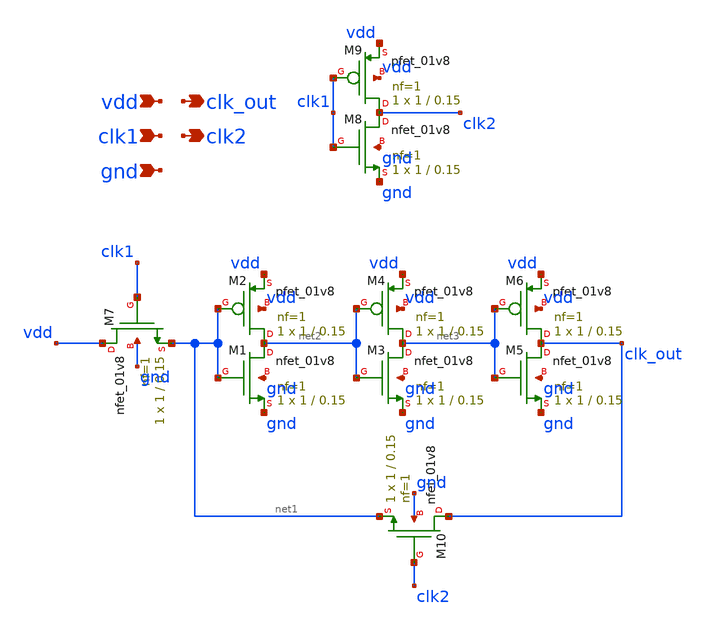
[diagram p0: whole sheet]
** sch_path: week3/xschem/ring_osc.sch
**.subckt ring_osc vdd gnd clk1 clk_out clk2
*.ipin vdd
*.ipin gnd
*.ipin clk1
*.opin clk_out
*.opin clk2
XM1 net2 net1 gnd gnd sky130_fd_pr__nfet_01v8 L=0.15 W=1 nf=1 ad='int((nf+1)/2) * W/nf * 0.29' as='int((nf+2)/2) * W/nf * 0.29'
+ pd='2*int((nf+1)/2) * (W/nf + 0.29)' ps='2*int((nf+2)/2) * (W/nf + 0.29)' nrd='0.29 / W' nrs='0.29 / W'
+ sa=0 sb=0 sd=0 mult=1 m=1
XM2 net2 net1 vdd vdd sky130_fd_pr__pfet_01v8 L=0.15 W=1 nf=1 ad='int((nf+1)/2) * W/nf * 0.29' as='int((nf+2)/2) * W/nf * 0.29'
+ pd='2*int((nf+1)/2) * (W/nf + 0.29)' ps='2*int((nf+2)/2) * (W/nf + 0.29)' nrd='0.29 / W' nrs='0.29 / W'
+ sa=0 sb=0 sd=0 mult=1 m=1
XM3 net3 net2 gnd gnd sky130_fd_pr__nfet_01v8 L=0.15 W=1 nf=1 ad='int((nf+1)/2) * W/nf * 0.29' as='int((nf+2)/2) * W/nf * 0.29'
+ pd='2*int((nf+1)/2) * (W/nf + 0.29)' ps='2*int((nf+2)/2) * (W/nf + 0.29)' nrd='0.29 / W' nrs='0.29 / W'
+ sa=0 sb=0 sd=0 mult=1 m=1
XM4 net3 net2 vdd vdd sky130_fd_pr__pfet_01v8 L=0.15 W=1 nf=1 ad='int((nf+1)/2) * W/nf * 0.29' as='int((nf+2)/2) * W/nf * 0.29'
+ pd='2*int((nf+1)/2) * (W/nf + 0.29)' ps='2*int((nf+2)/2) * (W/nf + 0.29)' nrd='0.29 / W' nrs='0.29 / W'
+ sa=0 sb=0 sd=0 mult=1 m=1
XM5 clk_out net3 gnd gnd sky130_fd_pr__nfet_01v8 L=0.15 W=1 nf=1 ad='int((nf+1)/2) * W/nf * 0.29' as='int((nf+2)/2) * W/nf * 0.29'
+ pd='2*int((nf+1)/2) * (W/nf + 0.29)' ps='2*int((nf+2)/2) * (W/nf + 0.29)' nrd='0.29 / W' nrs='0.29 / W'
+ sa=0 sb=0 sd=0 mult=1 m=1
XM6 clk_out net3 vdd vdd sky130_fd_pr__pfet_01v8 L=0.15 W=1 nf=1 ad='int((nf+1)/2) * W/nf * 0.29' as='int((nf+2)/2) * W/nf * 0.29'
+ pd='2*int((nf+1)/2) * (W/nf + 0.29)' ps='2*int((nf+2)/2) * (W/nf + 0.29)' nrd='0.29 / W' nrs='0.29 / W'
+ sa=0 sb=0 sd=0 mult=1 m=1
XM7 vdd clk1 net1 gnd sky130_fd_pr__nfet_01v8 L=0.15 W=1 nf=1 ad='int((nf+1)/2) * W/nf * 0.29' as='int((nf+2)/2) * W/nf * 0.29'
+ pd='2*int((nf+1)/2) * (W/nf + 0.29)' ps='2*int((nf+2)/2) * (W/nf + 0.29)' nrd='0.29 / W' nrs='0.29 / W'
+ sa=0 sb=0 sd=0 mult=1 m=1
XM8 clk2 clk1 gnd gnd sky130_fd_pr__nfet_01v8 L=0.15 W=1 nf=1 ad='int((nf+1)/2) * W/nf * 0.29' as='int((nf+2)/2) * W/nf * 0.29'
+ pd='2*int((nf+1)/2) * (W/nf + 0.29)' ps='2*int((nf+2)/2) * (W/nf + 0.29)' nrd='0.29 / W' nrs='0.29 / W'
+ sa=0 sb=0 sd=0 mult=1 m=1
XM9 clk2 clk1 vdd vdd sky130_fd_pr__pfet_01v8 L=0.15 W=1 nf=1 ad='int((nf+1)/2) * W/nf * 0.29' as='int((nf+2)/2) * W/nf * 0.29'
+ pd='2*int((nf+1)/2) * (W/nf + 0.29)' ps='2*int((nf+2)/2) * (W/nf + 0.29)' nrd='0.29 / W' nrs='0.29 / W'
+ sa=0 sb=0 sd=0 mult=1 m=1
XM10 clk_out clk2 net1 gnd sky130_fd_pr__nfet_01v8 L=0.15 W=1 nf=1 ad='int((nf+1)/2) * W/nf * 0.29' as='int((nf+2)/2) * W/nf * 0.29'
+ pd='2*int((nf+1)/2) * (W/nf + 0.29)' ps='2*int((nf+2)/2) * (W/nf + 0.29)' nrd='0.29 / W' nrs='0.29 / W'
+ sa=0 sb=0 sd=0 mult=1 m=1
**.ends
.end
